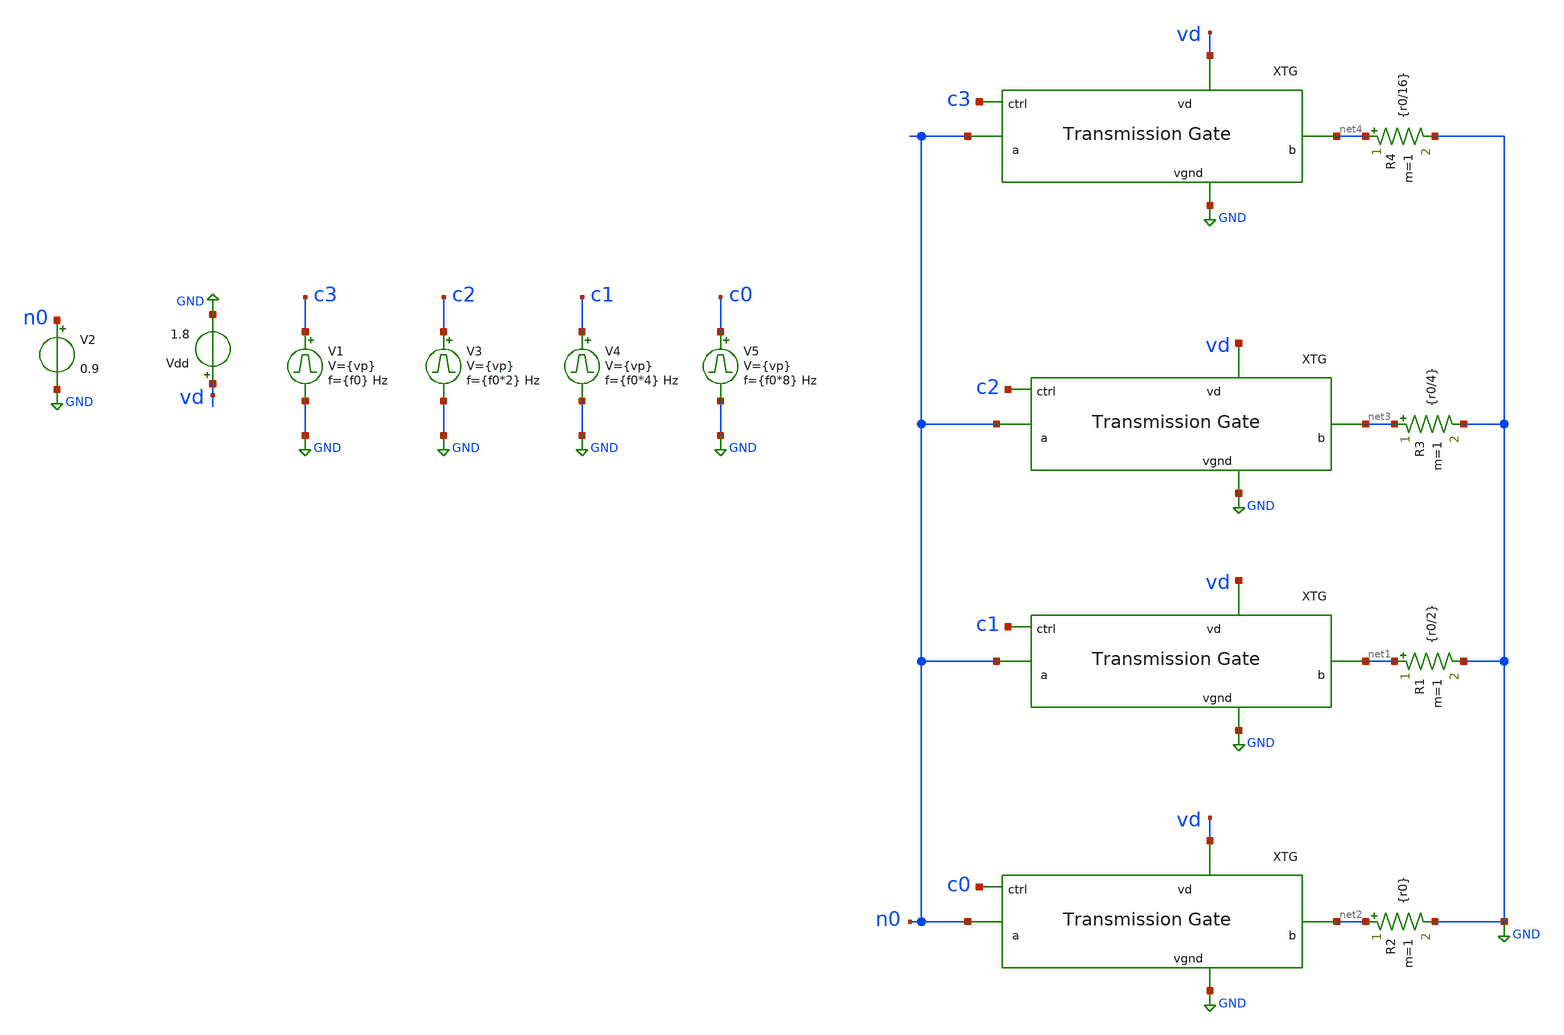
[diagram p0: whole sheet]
** sch_path: xschem/n-tg-tb.sch
**.subckt n-tg-tb
Vdd vd GND 1.8
V1 c3 GND pulse 0 {vp} '0.495/ {f0} ' '0.01/{f0} ' '0.01/{f0} ' '0.49/{f0} ' '1/{f0} '
V2 n0 GND 0.9
x9 c0 vd net2 GND n0 tg
x10 c1 vd net1 GND n0 tg
x7 c2 vd net3 GND n0 tg
x8 c3 vd net4 GND n0 tg
R1 net1 GND {r0/2} m=1
R2 net2 GND {r0} m=1
R3 net3 GND {r0/4} m=1
R4 net4 GND {r0/16} m=1
V3 c2 GND pulse 0 {vp} '0.495/ {f0*2} ' '0.01/{f0*2} ' '0.01/{f0*2} ' '0.49/{f0*2} ' '1/{f0*2} '
V4 c1 GND pulse 0 {vp} '0.495/ {f0*4} ' '0.01/{f0*4} ' '0.01/{f0*4} ' '0.49/{f0*4} ' '1/{f0*4} '
V5 c0 GND pulse 0 {vp} '0.495/ {f0*8} ' '0.01/{f0*8} ' '0.01/{f0*8} ' '0.49/{f0*8} ' '1/{f0*8} '
**** begin user architecture code


.param f0=1 vp=1.8 r0=20k

.control

destroy all
set color0=white
set color1=black
save all
tran 1m 1

let r = abs(n0/i(V2))
*let scale = maximum(r_total)/(4*1.8+3*0.2)
let scale = 20k/(4*1.8+3*0.2)
plot r
plot c0*scale c1*scale+2*scale c2*scale+4*scale c3*scale+6*scale r ylimit 0 20k*0.1
.endc

 .lib $::SKYWATER_MODELS/sky130.lib.spice tt
.include $::SKYWATER_STDCELLS/sky130_fd_sc_hd.spice

**** end user architecture code
**.ends

* expanding   symbol:  projects/dpga-ieee-sscs-contest/xschem/tg.sym # of pins=5
** sym_path: projects/dpga-ieee-sscs-contest/xschem/tg.sym
** sch_path: projects/dpga-ieee-sscs-contest/xschem/tg.sch
.subckt tg ctrl vd b vgnd a
*.iopin vd
*.iopin vgnd
*.iopin b
*.iopin a
*.ipin ctrl
XM2 b nctrl a vd sky130_fd_pr__pfet_01v8 L=0.15 W=60 nf=12 ad='int((nf+1)/2) * W/nf * 0.29' as='int((nf+2)/2) * W/nf * 0.29'
+ pd='2*int((nf+1)/2) * (W/nf + 0.29)' ps='2*int((nf+2)/2) * (W/nf + 0.29)' nrd='0.29 / W' nrs='0.29 / W'
+ sa=0 sb=0 sd=0 mult=1 m=1
XM1 a ctrl b vgnd sky130_fd_pr__nfet_01v8 L=0.15 W=60 nf=12 ad='int((nf+1)/2) * W/nf * 0.29' as='int((nf+2)/2) * W/nf * 0.29'
+ pd='2*int((nf+1)/2) * (W/nf + 0.29)' ps='2*int((nf+2)/2) * (W/nf + 0.29)' nrd='0.29 / W' nrs='0.29 / W'
+ sa=0 sb=0 sd=0 mult=1 m=1
XM3 nctrl ctrl vgnd vgnd sky130_fd_pr__nfet_01v8 L=0.15 W=1 nf=1 ad='int((nf+1)/2) * W/nf * 0.29' as='int((nf+2)/2) * W/nf * 0.29'
+ pd='2*int((nf+1)/2) * (W/nf + 0.29)' ps='2*int((nf+2)/2) * (W/nf + 0.29)' nrd='0.29 / W' nrs='0.29 / W'
+ sa=0 sb=0 sd=0 mult=1 m=1
XM4 nctrl ctrl vd vd sky130_fd_pr__pfet_01v8 L=0.15 W=3 nf=1 ad='int((nf+1)/2) * W/nf * 0.29' as='int((nf+2)/2) * W/nf * 0.29'
+ pd='2*int((nf+1)/2) * (W/nf + 0.29)' ps='2*int((nf+2)/2) * (W/nf + 0.29)' nrd='0.29 / W' nrs='0.29 / W'
+ sa=0 sb=0 sd=0 mult=1 m=1
.ends

.GLOBAL GND
.end
